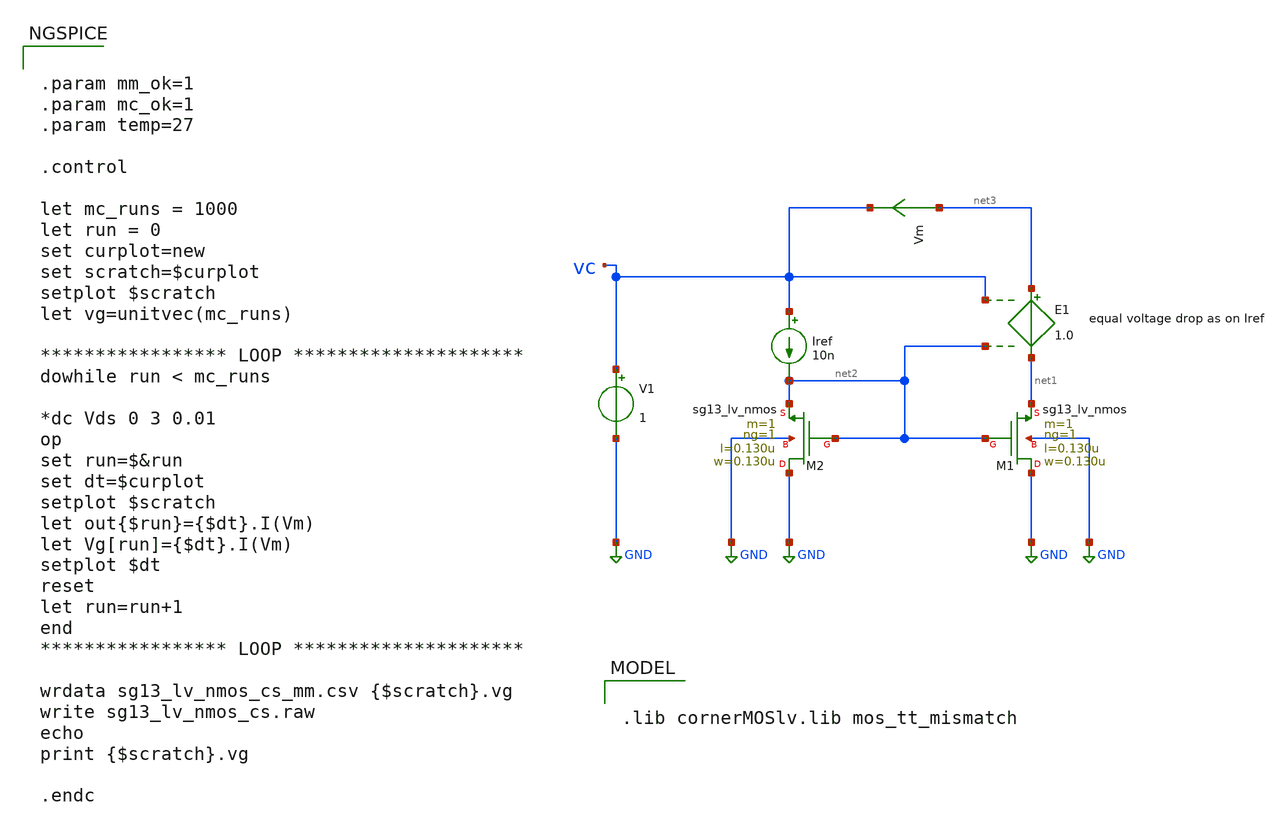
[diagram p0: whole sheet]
** sch_path: ihp-sg13g2/libs.tech/xschem/sg13g2_tests/mm_lv_nmos_cs_loop.sch
* Copyright 2023 IHP PDK Authors
**.subckt mm_lv_nmos_cs_loop
Iref vc net2 10n
XM1 GND net2 net1 GND sg13_lv_nmos w=0.130u l=0.130u ng=1 m=1
XM2 GND net2 net2 GND sg13_lv_nmos w=0.130u l=0.130u ng=1 m=1
E1 net3 net1 vc net2 1.0
Vm net3 vc 0
.save i(vm)
V1 vc GND 1
**** begin user architecture code

.lib cornerMOSlv.lib mos_tt_mismatch




.param mm_ok=1
.param mc_ok=1
.param temp=27

.control

let mc_runs = 1000
let run = 0
set curplot=new
set scratch=$curplot
setplot $scratch
let vg=unitvec(mc_runs)

***************** LOOP *********************
dowhile run < mc_runs

*dc Vds 0 3 0.01
op
set run=$&run
set dt=$curplot
setplot $scratch
let out{$run}={$dt}.I(Vm)
let Vg[run]={$dt}.I(Vm)
setplot $dt
reset
let run=run+1
end
***************** LOOP *********************

wrdata sg13_lv_nmos_cs_mm.csv {$scratch}.vg
write sg13_lv_nmos_cs.raw
echo
print {$scratch}.vg

.endc


**** end user architecture code
**.ends
.GLOBAL GND
.end
